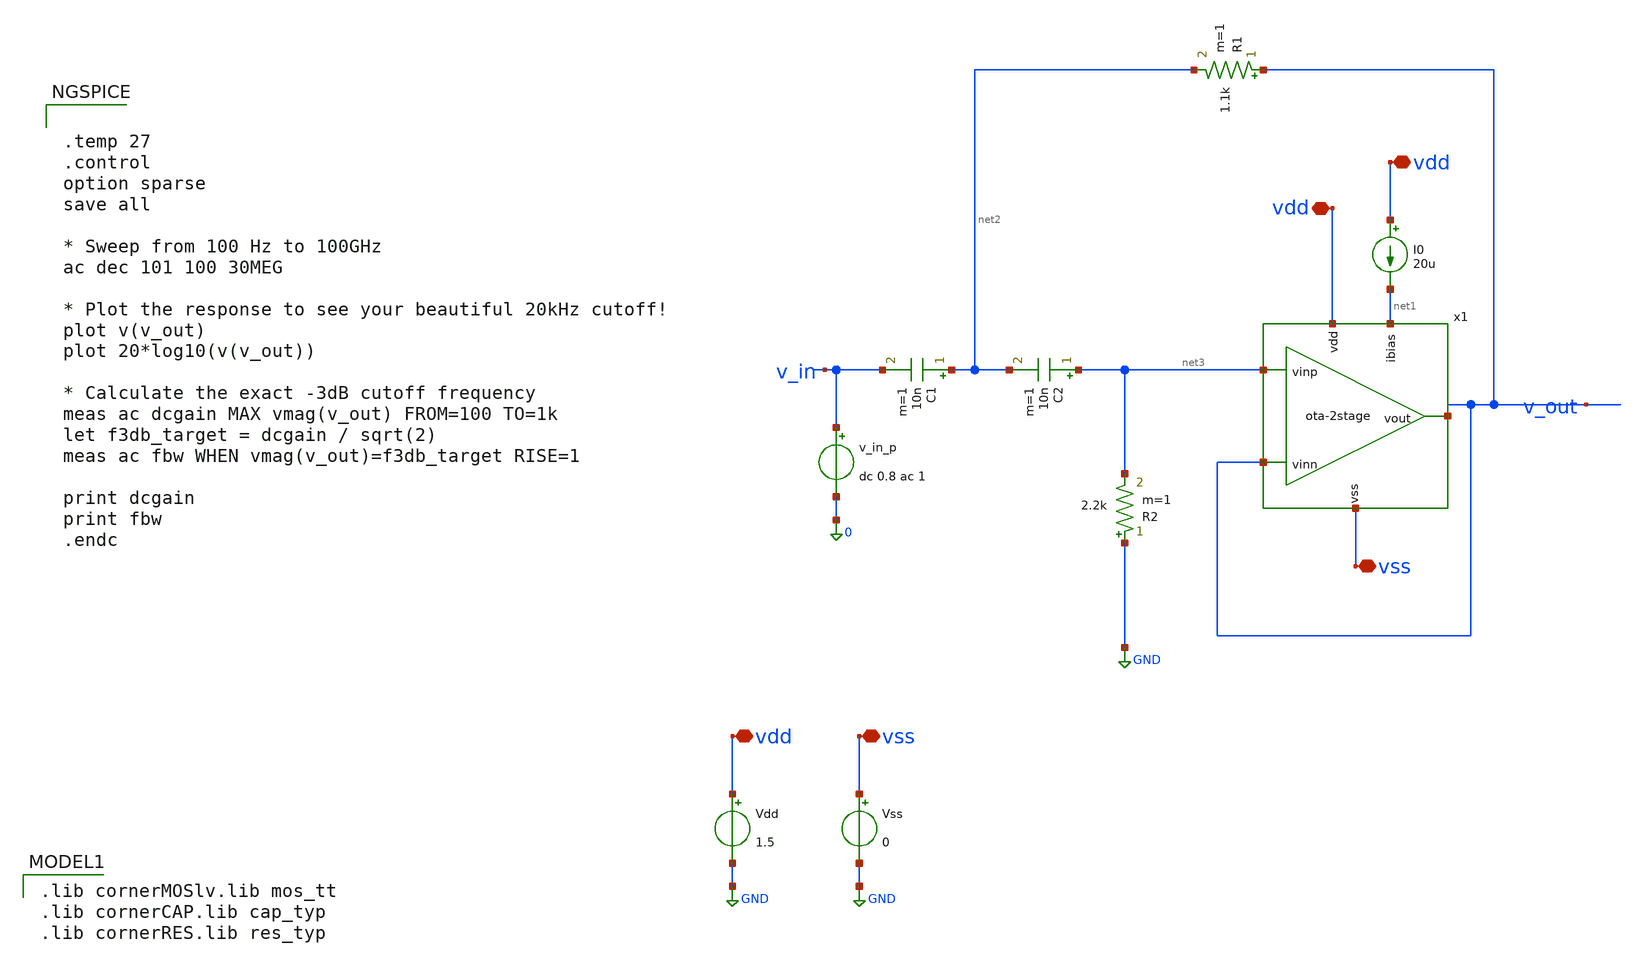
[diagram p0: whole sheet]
** sch_path: Testbench/ota-2stage_tb-sk-hpf.sch
**.subckt ota-2stage_tb-sk-hpf vdd vdd vdd vss vss
*.iopin vdd
*.iopin vdd
*.iopin vdd
*.iopin vss
*.iopin vss
I0 vdd net1 20u
Vdd vdd GND 1.5
Vss vss GND 0
v_in_p v_in 0 dc 0.8 ac 1
x1 vdd net1 v_out net4 net3 vss ota-2stage
R1 v_out net2 1.1k m=1
R2 GND net3 2.2k m=1
C1 net2 v_in 10n m=1
C2 net3 net2 10n m=1
**** begin user architecture code


.temp 27
.control
option sparse
save all

* Sweep from 100 Hz to 100GHz
ac dec 101 100 30MEG

* Plot the response to see your beautiful 20kHz cutoff!
plot v(v_out)
plot 20*log10(v(v_out))

* Calculate the exact -3dB cutoff frequency
meas ac dcgain MAX vmag(v_out) FROM=100 TO=1k
let f3db_target = dcgain / sqrt(2)
meas ac fbw WHEN vmag(v_out)=f3db_target RISE=1

print dcgain
print fbw
.endc


 .lib cornerMOSlv.lib mos_tt
.lib cornerCAP.lib cap_typ
.lib cornerRES.lib res_typ

**** end user architecture code
**.ends

* expanding   symbol:  ota-2stage.sym # of pins=6
** sym_path: Testbench/ota-2stage.sym
** sch_path: Testbench/ota-2stage.sch
.subckt ota-2stage vdd ibias vinn vout vinp vss
*.iopin vdd
*.iopin vss
*.ipin ibias
*.iopin vout
*.ipin vinn
*.ipin vinp
XM1 net1 vinn net3 net3 sg13_lv_nmos w=0.5u l=2u ng=1 m=1 mm_ok=1
XM2 net2 vinp net3 net3 sg13_lv_nmos w=0.5u l=2u ng=1 m=1 mm_ok=1
XM4 net2 net1 vdd vdd sg13_lv_pmos w=1u l=2u ng=1 m=1 mm_ok=1
XM3 net1 net1 vdd vdd sg13_lv_pmos w=1u l=2u ng=1 m=1 mm_ok=1
XM5 vout net2 vdd vdd sg13_lv_pmos w=4.5u l=2u ng=1 m=1 mm_ok=1
XM6 ibias ibias vss vss sg13_lv_nmos w=2u l=2u ng=1 m=1 mm_ok=1
XM7 net3 ibias vss vss sg13_lv_nmos w=0.5u l=2u ng=1 m=1 mm_ok=1
XM8 vout ibias vss vss sg13_lv_nmos w=0.5u l=2u ng=1 m=1 mm_ok=1
XCM vout net4 cap_cmim w=11.8e-6 l=11.8e-6 m=1 mm_ok=1
XRN net2 net4 GND rhigh w=1e-6 l=17e-6 m=1 b=0 mm_ok=1
.ends

.GLOBAL GND
.end
